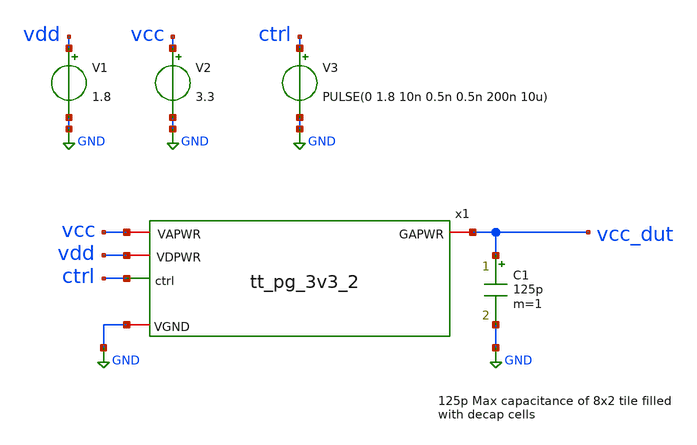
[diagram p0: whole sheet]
** sch_path: pg/tt_pg_3v3_2/xschem/tb_switch.sch
**.subckt tb_switch
x1 GND vdd vcc ctrl vcc_dut tt_pg_3v3_2
V2 vcc GND 3.3
.save i(v2)
V3 ctrl GND PULSE(0 1.8 10n 0.5n 0.5n 200n 10u)
V1 vdd GND 1.8
.save i(v1)
C1 vcc_dut GND 125p m=1
**** begin user architecture code

** opencircuitdesign pdks install
.lib $::SKYWATER_MODELS/sky130.lib.spice tt
.include $::SKYWATER_STDCELLS/sky130_fd_sc_hd.spice





.param mc_mm_switch=0
.control
save all
tran 100p 5u
plot ctrl x1.H_ctrl x1.H_ctrl_n x1.pmos_gate vcc_dut xlimit 9n 20n
plot ctrl x1.H_ctrl x1.H_ctrl_n x1.pmos_gate vcc_dut xlimit 209n 220n
plot vcc_dut
plot i(v.x1.vdischg)
*quit 0
.endc
.end


**** end user architecture code
**.ends
.GLOBAL GND
.end
